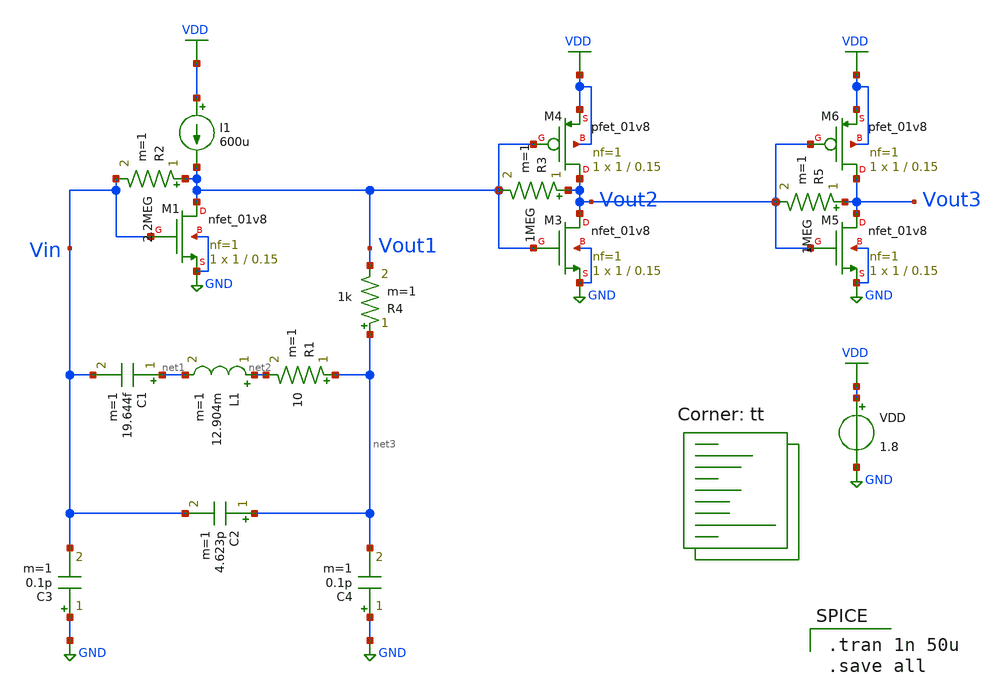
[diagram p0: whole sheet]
** sch_path: pll/xctl_lib/xctl/xschem/schematic_crystal.sch
**.subckt schematic_crystal
L1 net2 net1 12.904m m=1
XM1 Vout1 Vin GND GND sky130_fd_pr__nfet_01v8 L=0.15 W=1 nf=1 ad='int((nf+1)/2) * W/nf * 0.29' as='int((nf+2)/2) * W/nf * 0.29'
+ pd='2*int((nf+1)/2) * (W/nf + 0.29)' ps='2*int((nf+2)/2) * (W/nf + 0.29)' nrd='0.29 / W' nrs='0.29 / W'
+ sa=0 sb=0 sd=0 mult=1 m=1
C3 GND Vin 0.1p m=1
C4 GND net3 0.1p m=1
VDD VDD GND 1.8
R2 Vout1 Vin 2.2MEG m=1
XM3 Vout2 Vout1 GND GND sky130_fd_pr__nfet_01v8 L=0.15 W=1 nf=1 ad='int((nf+1)/2) * W/nf * 0.29' as='int((nf+2)/2) * W/nf * 0.29'
+ pd='2*int((nf+1)/2) * (W/nf + 0.29)' ps='2*int((nf+2)/2) * (W/nf + 0.29)' nrd='0.29 / W' nrs='0.29 / W'
+ sa=0 sb=0 sd=0 mult=1 m=1
XM4 Vout2 Vout1 VDD VDD sky130_fd_pr__pfet_01v8 L=0.15 W=1 nf=1 ad='int((nf+1)/2) * W/nf * 0.29' as='int((nf+2)/2) * W/nf * 0.29'
+ pd='2*int((nf+1)/2) * (W/nf + 0.29)' ps='2*int((nf+2)/2) * (W/nf + 0.29)' nrd='0.29 / W' nrs='0.29 / W'
+ sa=0 sb=0 sd=0 mult=1 m=1
R3 Vout2 Vout1 1MEG m=1
C1 net1 Vin 19.644f m=1
R1 net3 net2 10 m=1
C2 net3 Vin 4.623p m=1
XM5 Vout3 Vout2 GND GND sky130_fd_pr__nfet_01v8 L=0.15 W=1 nf=1 ad='int((nf+1)/2) * W/nf * 0.29' as='int((nf+2)/2) * W/nf * 0.29'
+ pd='2*int((nf+1)/2) * (W/nf + 0.29)' ps='2*int((nf+2)/2) * (W/nf + 0.29)' nrd='0.29 / W' nrs='0.29 / W'
+ sa=0 sb=0 sd=0 mult=1 m=1
XM6 Vout3 Vout2 VDD VDD sky130_fd_pr__pfet_01v8 L=0.15 W=1 nf=1 ad='int((nf+1)/2) * W/nf * 0.29' as='int((nf+2)/2) * W/nf * 0.29'
+ pd='2*int((nf+1)/2) * (W/nf + 0.29)' ps='2*int((nf+2)/2) * (W/nf + 0.29)' nrd='0.29 / W' nrs='0.29 / W'
+ sa=0 sb=0 sd=0 mult=1 m=1
R5 Vout3 Vout2 1MEG m=1
I1 VDD Vout1 600u
R4 net3 Vout1 1k m=1
**** begin user architecture code

.tran 1n 50u
.save all

.lib $::SKYWATER_MODELS/sky130.lib.spice tt
**** end user architecture code
**.ends
.GLOBAL VDD
.GLOBAL GND
.end
